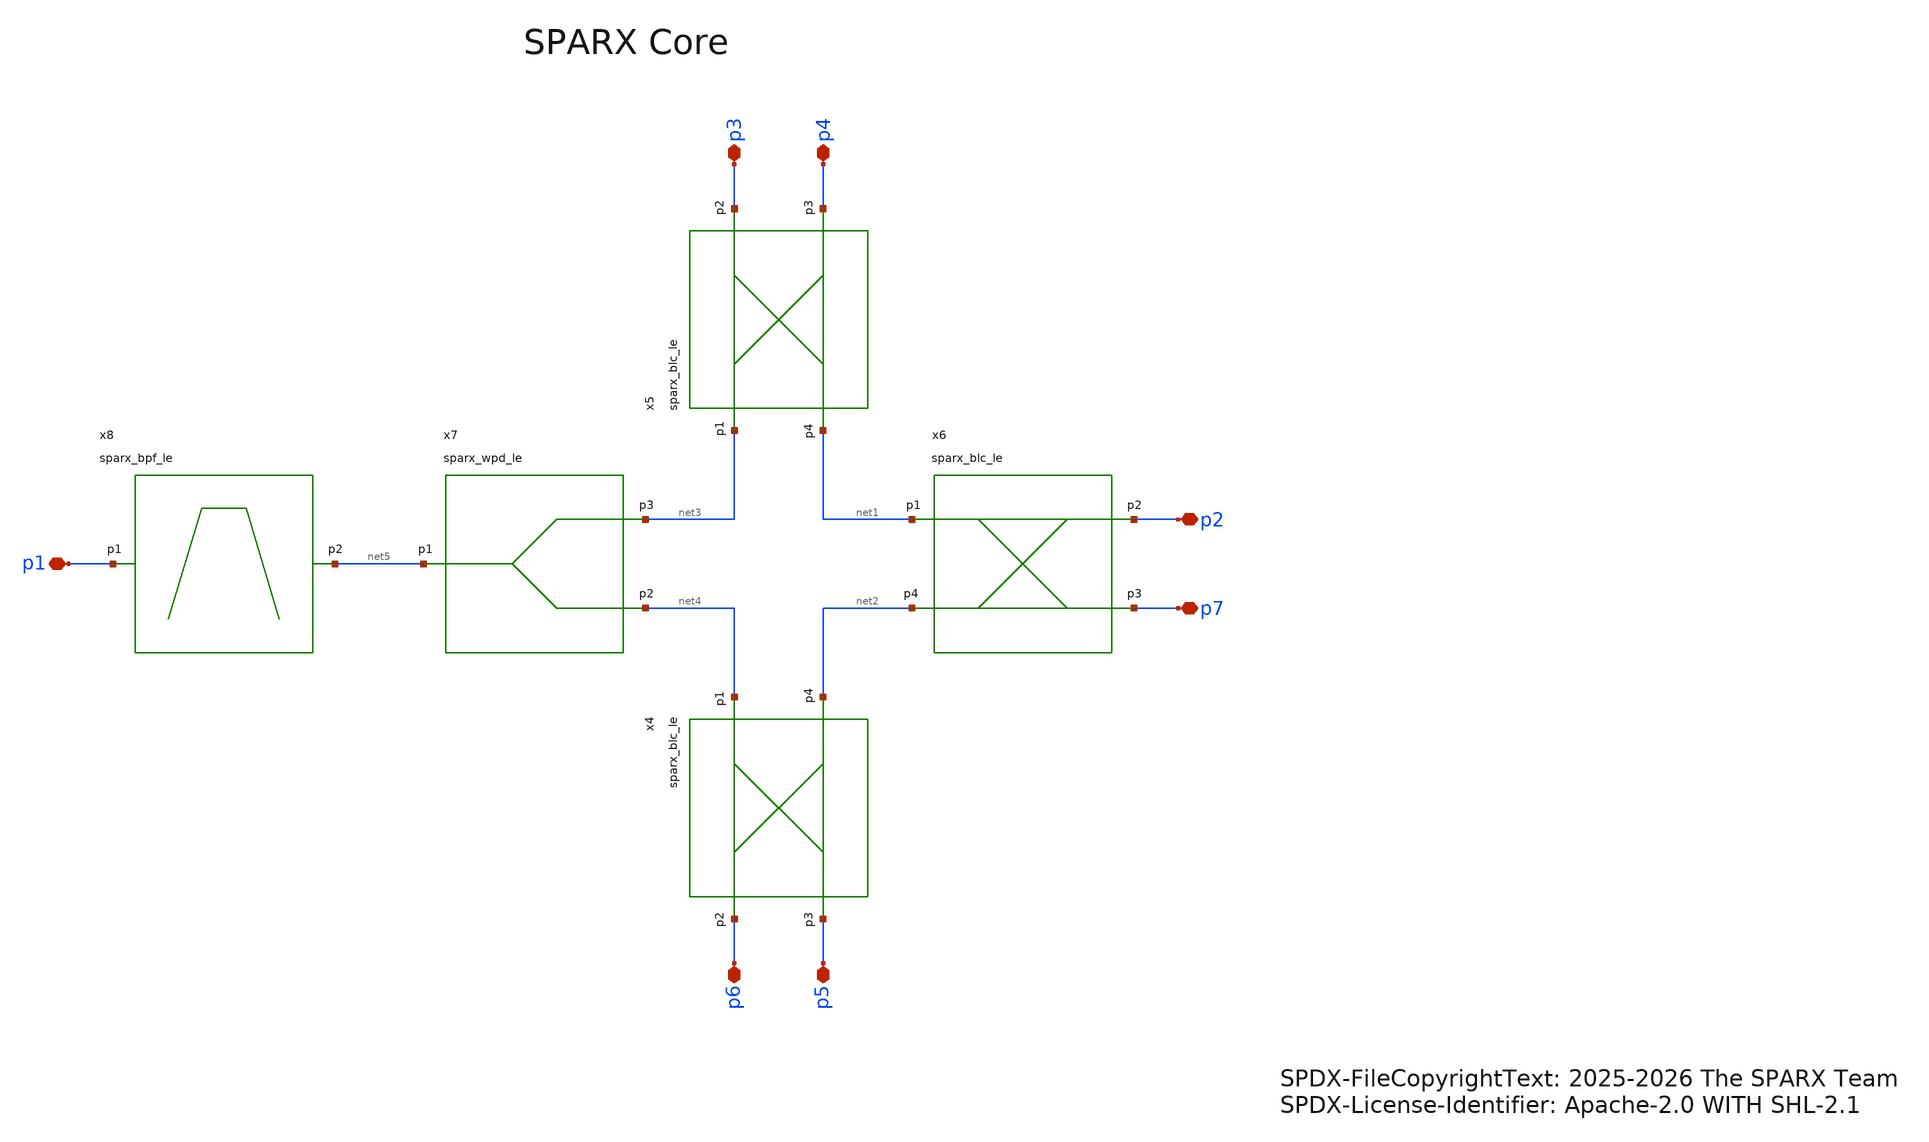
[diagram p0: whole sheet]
** sch_path: schematic/sparx_core.sch
* SPDX-FileCopyrightText: 2025-2026 The SPARX Team
* SPDX-License-Identifier: Apache-2.0 WITH SHL-2.1
**.subckt sparx_core p1 p3 p4 p2 p7 p6 p5
*.iopin p1
*.iopin p3
*.iopin p4
*.iopin p2
*.iopin p7
*.iopin p6
*.iopin p5
x5 net3 p3 p4 net1 sparx_blc_le
x6 net1 p2 p7 net2 sparx_blc_le
x7 net5 net4 net3 sparx_wpd_le
x8 p1 net5 sparx_bpf_le
x4 net4 p6 p5 net2 sparx_blc_le
**.ends
.end
